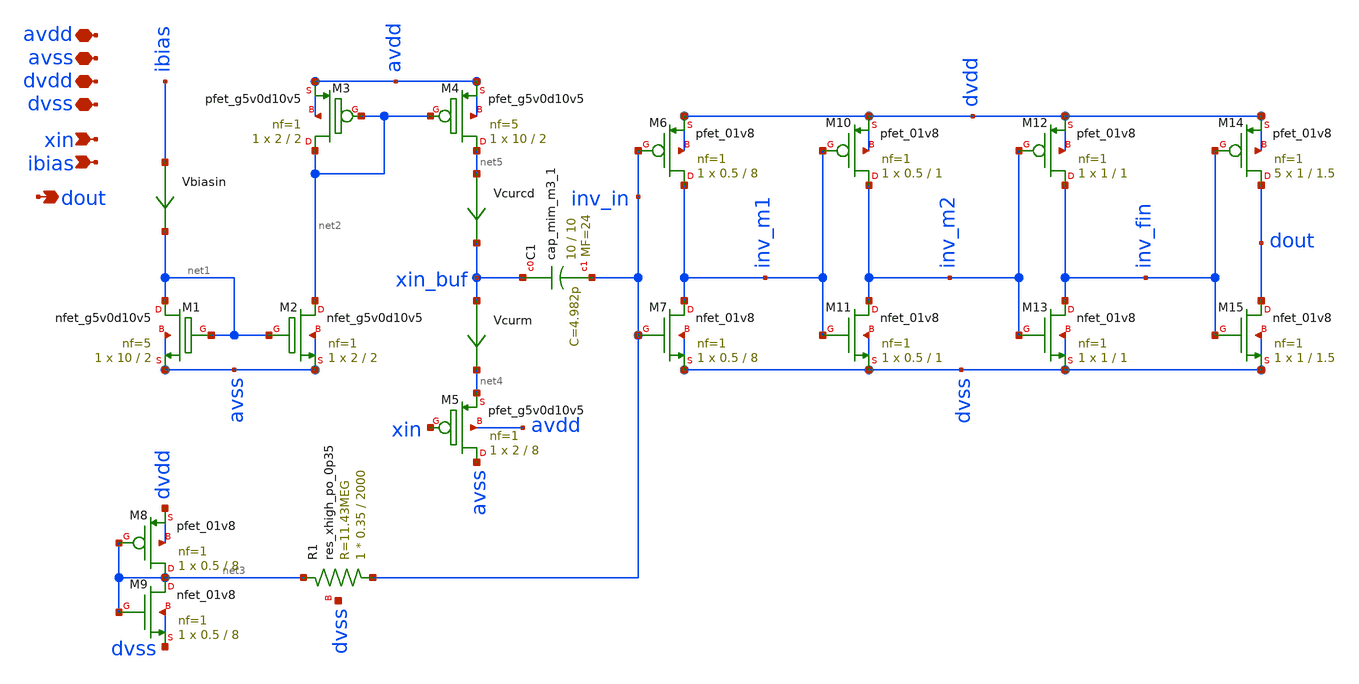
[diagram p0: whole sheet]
** sch_path: xschem/dout_amp.sch
**.subckt dout_amp xin avdd avss dvdd dvss dout ibias
*.ipin xin
*.iopin avdd
*.iopin avss
*.iopin dvdd
*.iopin dvss
*.opin dout
*.ipin ibias
XM3 net2 net2 avdd avdd sky130_fd_pr__pfet_g5v0d10v5 L=2 W=2 nf=1 ad='int((nf+1)/2) * W/nf * 0.29' as='int((nf+2)/2) * W/nf * 0.29'
+ pd='2*int((nf+1)/2) * (W/nf + 0.29)' ps='2*int((nf+2)/2) * (W/nf + 0.29)' nrd='0.29 / W' nrs='0.29 / W'
+ sa=0 sb=0 sd=0 mult=1 m=1
XM1 net1 net1 avss avss sky130_fd_pr__nfet_g5v0d10v5 L=2 W=10 nf=5 ad='int((nf+1)/2) * W/nf * 0.29' as='int((nf+2)/2) * W/nf * 0.29'
+ pd='2*int((nf+1)/2) * (W/nf + 0.29)' ps='2*int((nf+2)/2) * (W/nf + 0.29)' nrd='0.29 / W' nrs='0.29 / W'
+ sa=0 sb=0 sd=0 mult=1 m=1
XM2 net2 net1 avss avss sky130_fd_pr__nfet_g5v0d10v5 L=2 W=2 nf=1 ad='int((nf+1)/2) * W/nf * 0.29' as='int((nf+2)/2) * W/nf * 0.29'
+ pd='2*int((nf+1)/2) * (W/nf + 0.29)' ps='2*int((nf+2)/2) * (W/nf + 0.29)' nrd='0.29 / W' nrs='0.29 / W'
+ sa=0 sb=0 sd=0 mult=1 m=1
XM4 net5 net2 avdd avdd sky130_fd_pr__pfet_g5v0d10v5 L=2 W=10 nf=5 ad='int((nf+1)/2) * W/nf * 0.29' as='int((nf+2)/2) * W/nf * 0.29'
+ pd='2*int((nf+1)/2) * (W/nf + 0.29)' ps='2*int((nf+2)/2) * (W/nf + 0.29)' nrd='0.29 / W' nrs='0.29 / W'
+ sa=0 sb=0 sd=0 mult=1 m=1
XM5 avss xin net4 avdd sky130_fd_pr__pfet_g5v0d10v5 L=8 W=2 nf=1 ad='int((nf+1)/2) * W/nf * 0.29' as='int((nf+2)/2) * W/nf * 0.29'
+ pd='2*int((nf+1)/2) * (W/nf + 0.29)' ps='2*int((nf+2)/2) * (W/nf + 0.29)' nrd='0.29 / W' nrs='0.29 / W'
+ sa=0 sb=0 sd=0 mult=1 m=1
XC1 xin_buf inv_in sky130_fd_pr__cap_mim_m3_1 W=10 L=10 MF=24 m=24
XM6 inv_m1 inv_in dvdd dvdd sky130_fd_pr__pfet_01v8 L=8 W=0.5 nf=1 ad='int((nf+1)/2) * W/nf * 0.29' as='int((nf+2)/2) * W/nf * 0.29'
+ pd='2*int((nf+1)/2) * (W/nf + 0.29)' ps='2*int((nf+2)/2) * (W/nf + 0.29)' nrd='0.29 / W' nrs='0.29 / W'
+ sa=0 sb=0 sd=0 mult=1 m=1
XM7 inv_m1 inv_in dvss dvss sky130_fd_pr__nfet_01v8 L=8 W=0.5 nf=1 ad='int((nf+1)/2) * W/nf * 0.29' as='int((nf+2)/2) * W/nf * 0.29'
+ pd='2*int((nf+1)/2) * (W/nf + 0.29)' ps='2*int((nf+2)/2) * (W/nf + 0.29)' nrd='0.29 / W' nrs='0.29 / W'
+ sa=0 sb=0 sd=0 mult=1 m=1
XM8 net3 net3 dvdd dvdd sky130_fd_pr__pfet_01v8 L=8 W=0.5 nf=1 ad='int((nf+1)/2) * W/nf * 0.29' as='int((nf+2)/2) * W/nf * 0.29'
+ pd='2*int((nf+1)/2) * (W/nf + 0.29)' ps='2*int((nf+2)/2) * (W/nf + 0.29)' nrd='0.29 / W' nrs='0.29 / W'
+ sa=0 sb=0 sd=0 mult=1 m=1
XM9 net3 net3 dvss dvss sky130_fd_pr__nfet_01v8 L=8 W=0.5 nf=1 ad='int((nf+1)/2) * W/nf * 0.29' as='int((nf+2)/2) * W/nf * 0.29'
+ pd='2*int((nf+1)/2) * (W/nf + 0.29)' ps='2*int((nf+2)/2) * (W/nf + 0.29)' nrd='0.29 / W' nrs='0.29 / W'
+ sa=0 sb=0 sd=0 mult=1 m=1
XR1 inv_in net3 dvss sky130_fd_pr__res_xhigh_po_0p35 L=2000 mult=1 m=1
XM10 inv_m2 inv_m1 dvdd dvdd sky130_fd_pr__pfet_01v8 L=1 W=0.5 nf=1 ad='int((nf+1)/2) * W/nf * 0.29'
+ as='int((nf+2)/2) * W/nf * 0.29' pd='2*int((nf+1)/2) * (W/nf + 0.29)' ps='2*int((nf+2)/2) * (W/nf + 0.29)'
+ nrd='0.29 / W' nrs='0.29 / W' sa=0 sb=0 sd=0 mult=1 m=1
XM11 inv_m2 inv_m1 dvss dvss sky130_fd_pr__nfet_01v8 L=1 W=0.5 nf=1 ad='int((nf+1)/2) * W/nf * 0.29'
+ as='int((nf+2)/2) * W/nf * 0.29' pd='2*int((nf+1)/2) * (W/nf + 0.29)' ps='2*int((nf+2)/2) * (W/nf + 0.29)'
+ nrd='0.29 / W' nrs='0.29 / W' sa=0 sb=0 sd=0 mult=1 m=1
XM12 inv_fin inv_m2 dvdd dvdd sky130_fd_pr__pfet_01v8 L=1 W=1 nf=1 ad='int((nf+1)/2) * W/nf * 0.29' as='int((nf+2)/2) * W/nf * 0.29'
+ pd='2*int((nf+1)/2) * (W/nf + 0.29)' ps='2*int((nf+2)/2) * (W/nf + 0.29)' nrd='0.29 / W' nrs='0.29 / W'
+ sa=0 sb=0 sd=0 mult=1 m=1
XM13 inv_fin inv_m2 dvss dvss sky130_fd_pr__nfet_01v8 L=1 W=1 nf=1 ad='int((nf+1)/2) * W/nf * 0.29' as='int((nf+2)/2) * W/nf * 0.29'
+ pd='2*int((nf+1)/2) * (W/nf + 0.29)' ps='2*int((nf+2)/2) * (W/nf + 0.29)' nrd='0.29 / W' nrs='0.29 / W'
+ sa=0 sb=0 sd=0 mult=1 m=1
XM14 dout inv_fin dvdd dvdd sky130_fd_pr__pfet_01v8 L=1.5 W=1 nf=1 ad='int((nf+1)/2) * W/nf * 0.29' as='int((nf+2)/2) * W/nf * 0.29'
+ pd='2*int((nf+1)/2) * (W/nf + 0.29)' ps='2*int((nf+2)/2) * (W/nf + 0.29)' nrd='0.29 / W' nrs='0.29 / W'
+ sa=0 sb=0 sd=0 mult=5 m=5
XM15 dout inv_fin dvss dvss sky130_fd_pr__nfet_01v8 L=1.5 W=1 nf=1 ad='int((nf+1)/2) * W/nf * 0.29' as='int((nf+2)/2) * W/nf * 0.29'
+ pd='2*int((nf+1)/2) * (W/nf + 0.29)' ps='2*int((nf+2)/2) * (W/nf + 0.29)' nrd='0.29 / W' nrs='0.29 / W'
+ sa=0 sb=0 sd=0 mult=1 m=1
Vcurm xin_buf net4 0
.save i(vcurm)
Vcurcd net5 xin_buf 0
.save i(vcurcd)
Vbiasin ibias net1 0
.save i(vbiasin)
**.ends
.end
